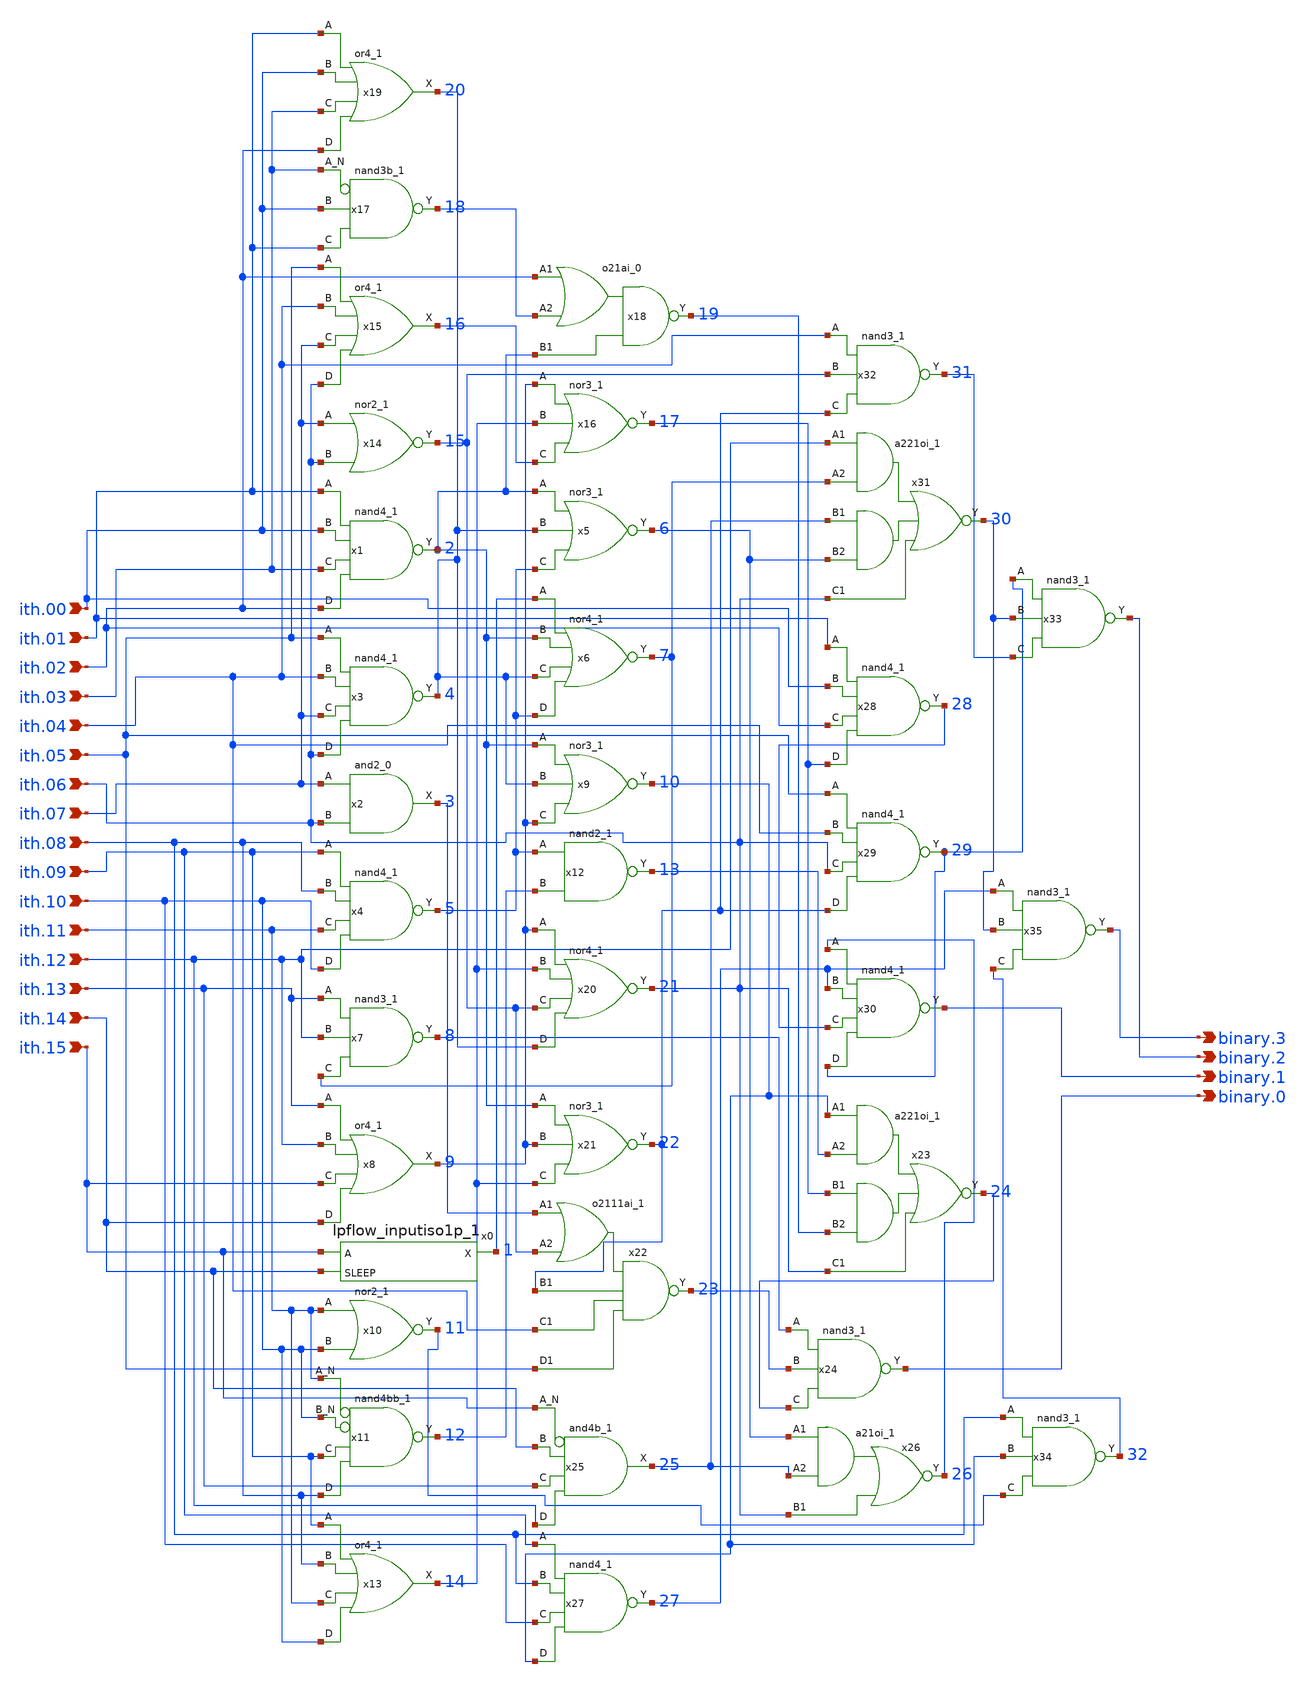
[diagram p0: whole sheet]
** sch_path: verilog/therm.sch
**.subckt therm ith.09 ith.13 ith.08 ith.10 ith.11 ith.14 ith.15 ith.12 ith.00 ith.01 ith.03 ith.04
*+ ith.05 ith.06 ith.02 ith.07 binary.0 binary.1 binary.2 binary.3
*.ipin ith.09
*.ipin ith.13
*.ipin ith.08
*.ipin ith.10
*.ipin ith.11
*.ipin ith.14
*.ipin ith.15
*.ipin ith.12
*.ipin ith.00
*.ipin ith.01
*.ipin ith.03
*.ipin ith.04
*.ipin ith.05
*.ipin ith.06
*.ipin ith.02
*.ipin ith.07
*.opin binary.0
*.opin binary.1
*.opin binary.2
*.opin binary.3
x0 ith.15 ith.14 VGND VNB VPB VPWR 1 sky130_fd_sc_hd__lpflow_inputiso1p_1
x1 ith.01 ith.00 ith.03 ith.02 VGND VNB VPB VPWR 2 sky130_fd_sc_hd__nand4_1
x2 ith.07 ith.06 VGND VNB VPB VPWR 3 sky130_fd_sc_hd__and2_0
x3 ith.05 ith.04 ith.07 ith.06 VGND VNB VPB VPWR 4 sky130_fd_sc_hd__nand4_1
x4 ith.09 ith.08 ith.11 ith.10 VGND VNB VPB VPWR 5 sky130_fd_sc_hd__nand4_1
x5 2 4 5 VGND VNB VPB VPWR 6 sky130_fd_sc_hd__nor3_1
x6 1 2 4 5 VGND VNB VPB VPWR 7 sky130_fd_sc_hd__nor4_1
x7 ith.13 ith.12 7 VGND VNB VPB VPWR 8 sky130_fd_sc_hd__nand3_1
x8 ith.13 ith.12 ith.15 ith.14 VGND VNB VPB VPWR 9 sky130_fd_sc_hd__or4_1
x9 2 4 9 VGND VNB VPB VPWR 10 sky130_fd_sc_hd__nor3_1
x10 ith.11 ith.10 VGND VNB VPB VPWR 11 sky130_fd_sc_hd__nor2_1
x11 ith.09 ith.08 VGND VNB VPB VPWR 12 sky130_fd_sc_hd__nand4bb_1
x12 5 12 VGND VNB VPB VPWR 13 sky130_fd_sc_hd__nand2_1
x13 ith.09 ith.08 ith.11 ith.10 VGND VNB VPB VPWR 14 sky130_fd_sc_hd__or4_1
x14 ith.07 ith.06 VGND VNB VPB VPWR 15 sky130_fd_sc_hd__nor2_1
x15 ith.05 ith.04 ith.07 ith.06 VGND VNB VPB VPWR 16 sky130_fd_sc_hd__or4_1
x16 9 14 16 VGND VNB VPB VPWR 17 sky130_fd_sc_hd__nor3_1
x17 ith.03 ith.00 ith.01 VGND VNB VPB VPWR 18 sky130_fd_sc_hd__nand3b_1
x18 ith.02 18 2 VGND VNB VPB VPWR 19 sky130_fd_sc_hd__o21ai_0
x19 ith.01 ith.00 ith.03 ith.02 VGND VNB VPB VPWR 4 sky130_fd_sc_hd__or4_1
x20 9 14 15 4 VGND VNB VPB VPWR ith.06 sky130_fd_sc_hd__nor4_1
x21 2 9 14 VGND VNB VPB VPWR 22 sky130_fd_sc_hd__nor3_1
x22 3 15 22 ith.04 ith.05 VGND VNB VPB VPWR 23 sky130_fd_sc_hd__o2111ai_1
x23 10 13 17 19 ith.06 VGND VNB VPB VPWR 24 sky130_fd_sc_hd__a221oi_1
x24 8 23 24 VGND VNB VPB VPWR binary.0 sky130_fd_sc_hd__nand3_1
x25 ith.15 ith.14 ith.13 ith.12 VGND VNB VPB VPWR 25 sky130_fd_sc_hd__and4b_1
x26 6 25 ith.06 VGND VNB VPB VPWR 26 sky130_fd_sc_hd__a21oi_1
x27 ith.09 ith.08 ith.10 10 VGND VNB VPB VPWR 27 sky130_fd_sc_hd__nand4_1
x28 ith.01 ith.00 ith.02 17 VGND VNB VPB VPWR 28 sky130_fd_sc_hd__nand4_1
x29 ith.05 ith.04 ith.06 22 VGND VNB VPB VPWR 29 sky130_fd_sc_hd__nand4_1
x30 26 27 28 29 VGND VNB VPB VPWR binary.1 sky130_fd_sc_hd__nand4_1
x31 ith.12 7 25 6 ith.06 VGND VNB VPB VPWR 30 sky130_fd_sc_hd__a221oi_1
x32 ith.04 15 22 VGND VNB VPB VPWR 31 sky130_fd_sc_hd__nand3_1
x33 29 30 31 VGND VNB VPB VPWR binary.2 sky130_fd_sc_hd__nand3_1
x34 ith.08 10 11 VGND VNB VPB VPWR 32 sky130_fd_sc_hd__nand3_1
x35 27 30 32 VGND VNB VPB VPWR binary.3 sky130_fd_sc_hd__nand3_1
**.ends
.end
